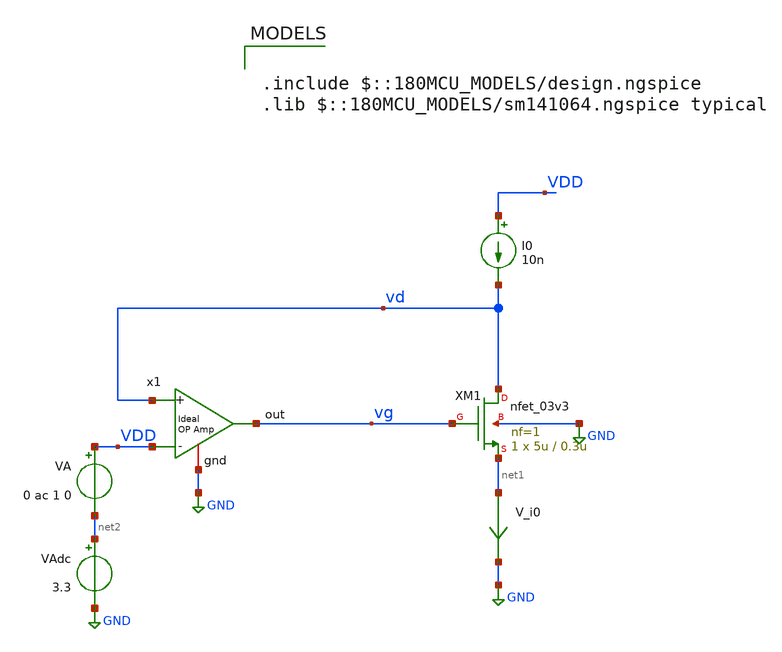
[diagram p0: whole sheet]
** sch_path: New_Extraction/nmos_sigma_ext.sch
**.subckt nmos_sigma_ext
x1 vg vd VDD GND ampOp_ideal
XM1 vd vg net1 GND nfet_03v3 L=0.3u W=5u nf=1 ad='int((nf+1)/2) * W/nf * 0.18u' as='int((nf+2)/2) * W/nf * 0.18u'
+ pd='2*int((nf+1)/2) * (W/nf + 0.18u)' ps='2*int((nf+2)/2) * (W/nf + 0.18u)' nrd='0.18u / W' nrs='0.18u / W'
+ sa=0 sb=0 sd=0 m=1
I0 VDD vd 10n
V_i0 net1 GND 0
.save i(v_i0)
VA VDD net2 0 ac 1 0
VAdc net2 GND 3.3
**** begin user architecture code

.include $::180MCU_MODELS/design.ngspice
.lib $::180MCU_MODELS/sm141064.ngspice typical



.option savecurrents

.control
  save all
  op
  remzerovec
  write nmos_sigma_ext.raw
  set appendwrite

  ac dec 100 1 1e10
  let sigma= -vg/vd
  let gm = i(v_i0)/vg

  meas ac sigma_at FIND sigma AT=10

  echo
  echo
  echo
  echo Extracted sigma:
  print sigma_at
  echo
  echo
  echo

  remzerovec
  write nmos_sigma_ext.raw


.endc
.save all


**** end user architecture code
**.ends

* expanding   symbol:  /home/gmaranhao/Desktop/gf180_work/auxLib/ampOp_ideal.sym # of pins=4
** sym_path: gf_tutorials/auxLib/ampOp_ideal.sym
** sch_path: gf_tutorials/auxLib/ampOp_ideal.sch
.subckt ampOp_ideal out + - gnd
*.ipin +
*.ipin -
*.opin out
*.iopin gnd
E1 out gnd + - 10000000
.ends

.GLOBAL GND
.end
